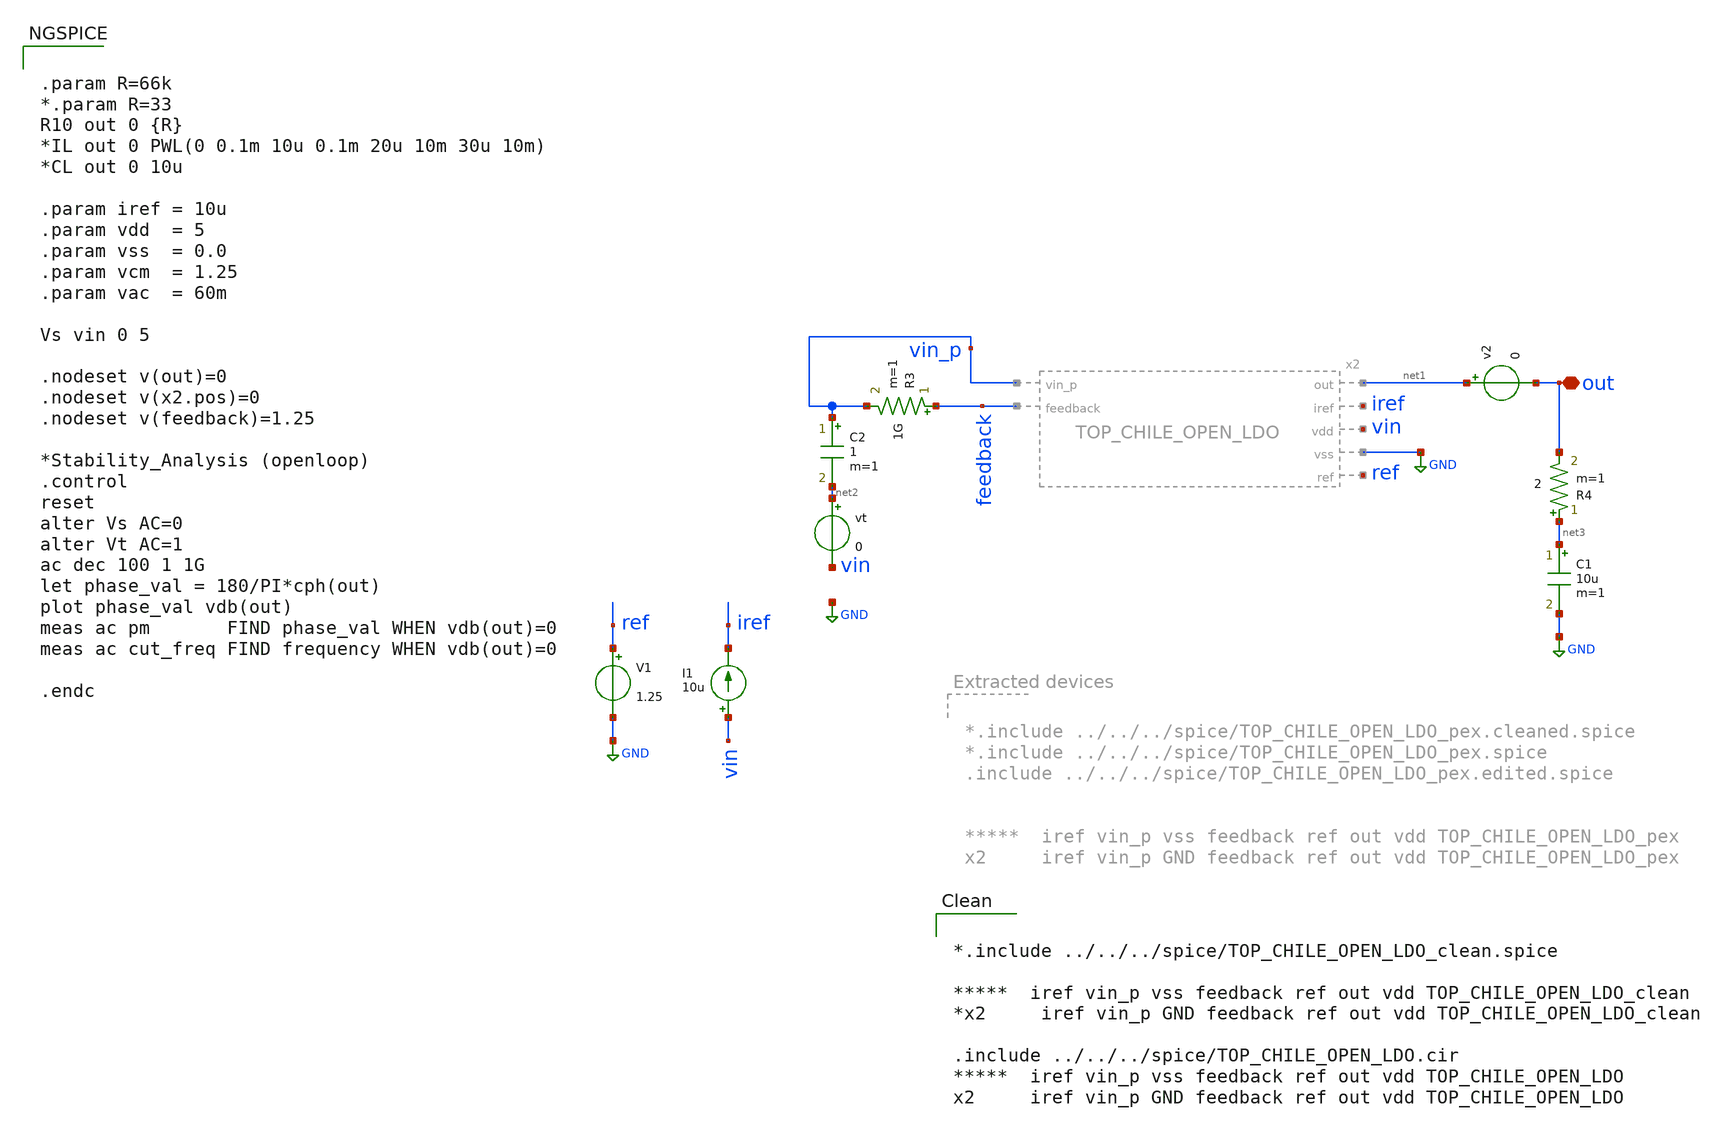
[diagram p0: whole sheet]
** sch_path: LDO/xschem/TOP_CHILE_OPEN_LDO/test/openloop.sch

.include $env(PDK_ROOT)/$env(PDK)/libs.tech/ngspice/design.ngspice
.lib $env(PDK_ROOT)/$env(PDK)/libs.tech/ngspice/sm141064.ngspice typical
.lib $env(PDK_ROOT)/$env(PDK)/libs.tech/ngspice/sm141064.ngspice res_typical

.lib $env(PDK_ROOT)/$env(PDK)/libs.tech/ngspice/sm141064.ngspice cap_mim
.lib $env(PDK_ROOT)/$env(PDK)/libs.tech/ngspice/sm141064.ngspice mimcap_typical

**.subckt openloop out
*.iopin out
I1 vin iref 10u
V1 ref GND 1.25
vt net2 vin 0
v2 net1 out 0
R3 feedback vin_p 1G m=1
C2 vin_p net2 1 m=1
C1 net3 GND 10u m=1
R4 net3 out 2 m=1
**** begin user architecture code


.param R=66k
*.param R=33
R10 out 0 {R}
*IL out 0 PWL(0 0.1m 10u 0.1m 20u 10m 30u 10m)
*CL out 0 10u

.param iref = 10u
.param vdd  = 5
.param vss  = 0.0
.param vcm  = 1.25
.param vac  = 60m

Vs vin 0 5

.nodeset v(out)=0
.nodeset v(x2.pos)=0
.nodeset v(feedback)=1.25

*Stability_Analysis (openloop)
.control
reset
alter Vs AC=0
alter Vt AC=1
ac dec 100 1 1G
let phase_val = 180/PI*cph(out)
plot phase_val vdb(out)
meas ac pm       FIND phase_val WHEN vdb(out)=0
meas ac cut_freq FIND frequency WHEN vdb(out)=0

.endc




*.include ../../../spice/TOP_CHILE_OPEN_LDO_clean.spice

*****  iref vin_p vss feedback ref out vdd TOP_CHILE_OPEN_LDO_clean
*x2     iref vin_p GND feedback ref out vdd TOP_CHILE_OPEN_LDO_clean

.include ../../../spice/TOP_CHILE_OPEN_LDO.cir
*****  iref vin_p vss feedback ref out vdd TOP_CHILE_OPEN_LDO
x2     iref vin_p GND feedback ref out vdd TOP_CHILE_OPEN_LDO


**** end user architecture code
**.ends
.GLOBAL GND
.end
